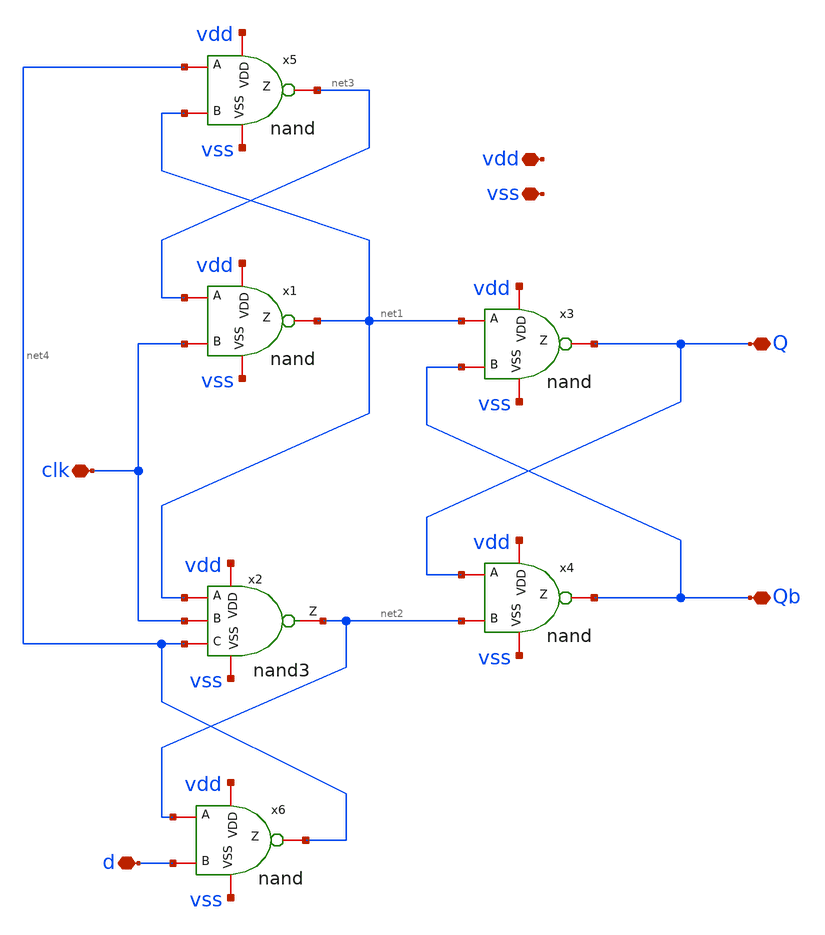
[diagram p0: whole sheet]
** sch_path: designs/libs/SIPO/dff.sch
**.subckt dff vdd vss Q Qb d clk
*.iopin vdd
*.iopin vss
*.iopin Q
*.iopin Qb
*.iopin d
*.iopin clk
x1 vdd net1 net3 clk vss nand
x3 vdd Q net1 Qb vss nand
x4 vdd Qb Q net2 vss nand
x2 vdd net2 net1 clk net4 vss nand3
x5 vdd net3 net4 net1 vss nand
x6 vdd net4 net2 d vss nand
**.ends
.end
